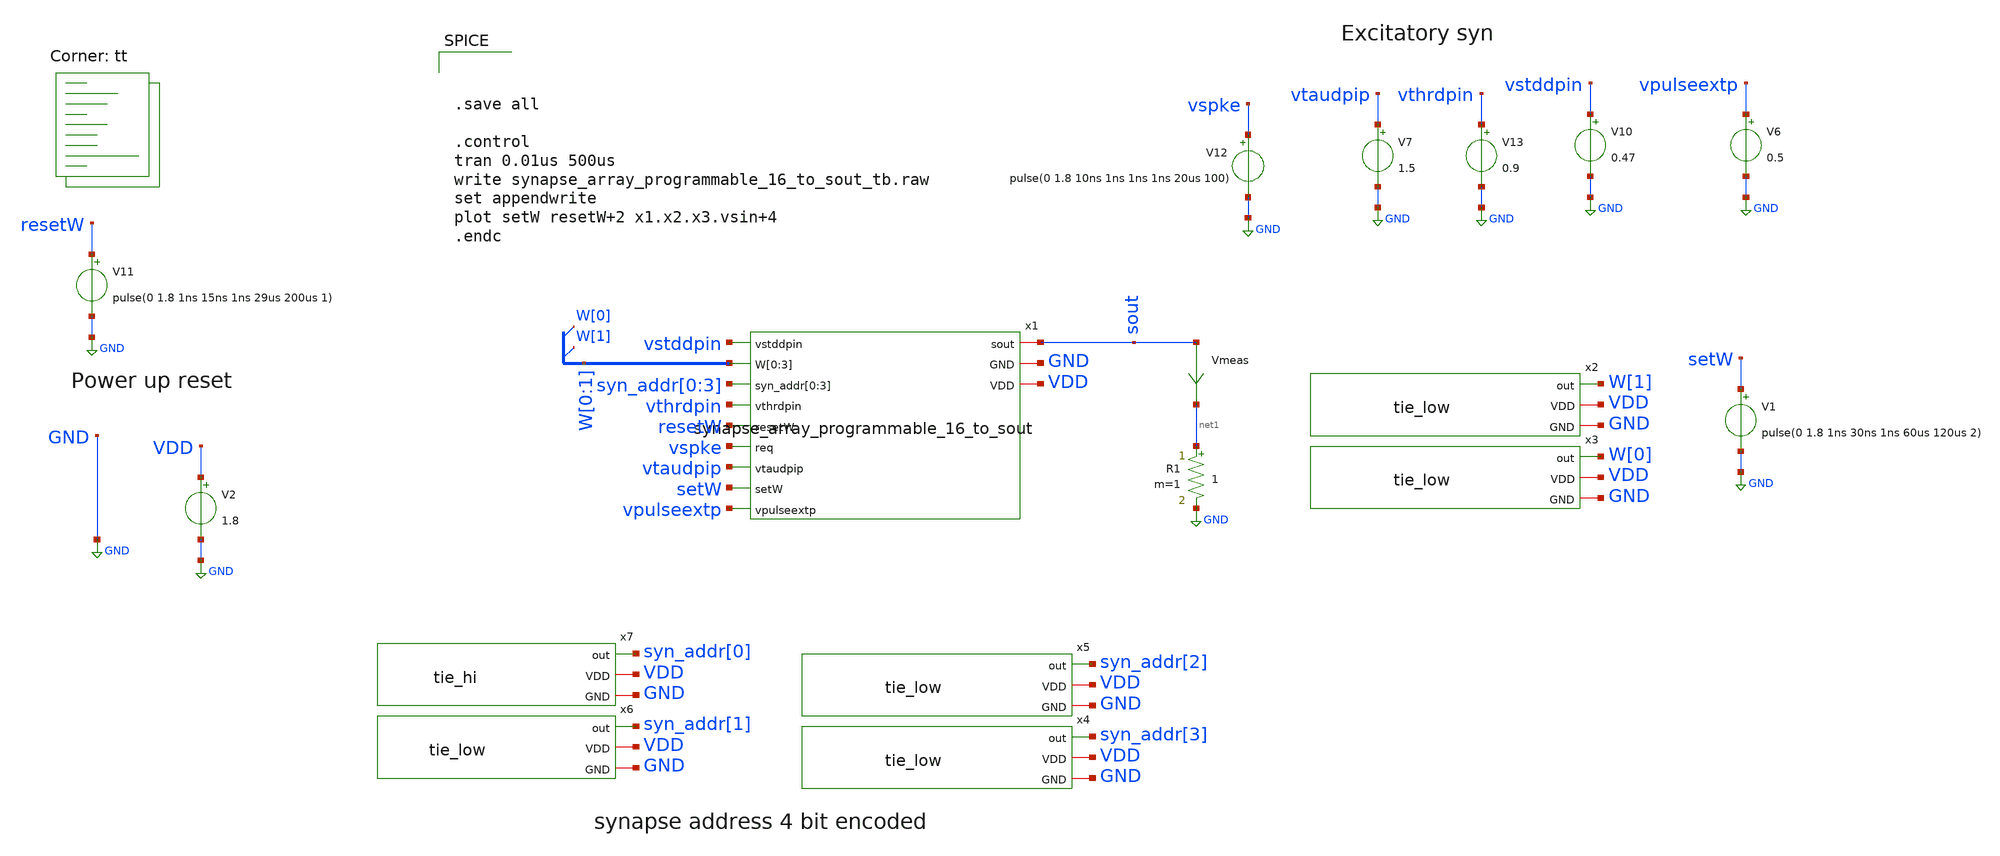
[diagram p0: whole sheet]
** sch_path: design/xschem/synapse_array_programmable_16_to_sout_tb.sch
**.subckt synapse_array_programmable_16_to_sout_tb
x1 vstddpin sout W[0] W[1] W[0] W[1] syn_addr[0] syn_addr[1] syn_addr[2] syn_addr[3] vthrdpin resetW
+ vspke vtaudpip setW vpulseextp GND VDD synapse_array_programmable_16_to_sout
R1 net1 GND 1 m=1
Vmeas sout net1 0
.save i(vmeas)
V11 resetW GND pulse(0 1.8 1ns 15ns 1ns 29us 200us 1)
V2 VDD GND 1.8
V7 vtaudpip GND 1.5
V13 vthrdpin GND 0.9
V10 vstddpin GND 0.47
V12 vspke GND pulse(0 1.8 10ns 1ns 1ns 1ns 20us 100)
V6 vpulseextp GND 0.5
V1 setW GND pulse(0 1.8 1ns 30ns 1ns 60us 120us 2)
x3 W[0] VDD GND tie_low
x2 W[1] VDD GND tie_low
x4 syn_addr[3] VDD GND tie_low
x5 syn_addr[2] VDD GND tie_low
x6 syn_addr[1] VDD GND tie_low
x7 syn_addr[0] VDD GND tie_hi
**** begin user architecture code



.save all

.control
tran 0.01us 500us
write synapse_array_programmable_16_to_sout_tb.raw
set appendwrite
plot setW resetW+2 x1.x2.x3.vsin+4
.endc




* Standard cell simulation files
.include $::SKYWATER_STDCELLS/sky130_fd_sc_hd.spice

* Power domains
VSTDCELL_PWR VPWR 0 DC 1.8
VSTDCELL_PB  VPB  0 DC 1.8
VSTDCELL_NB  VNB  0 DC 0
VSTDCELL_GND VGND 0 DC 0
.global VNB VGND VPB VPWR


.lib $::SKYWATER_MODELS/sky130.lib.spice tt
**** end user architecture code
**.ends

* expanding   symbol:  synapse_array_programmable_16_to_sout.sym # of pins=12
** sym_path: design/xschem/synapse_array_programmable_16_to_sout.sym
** sch_path: design/xschem/synapse_array_programmable_16_to_sout.sch
.subckt synapse_array_programmable_16_to_sout vstddpin sout W[0] W[1] W[2] W[3] syn_addr[0]
+ syn_addr[1] syn_addr[2] syn_addr[3] vthrdpin resetW req vtaudpip setW vpulseextp GND VDD
*.iopin GND
*.iopin VDD
*.ipin vpulseextp
*.ipin syn_addr[0],syn_addr[1],syn_addr[2],syn_addr[3]
*.ipin W[0],W[1],W[2],W[3]
*.ipin vthrdpin
*.ipin vtaudpip
*.ipin vstddpin
*.iopin sout
*.ipin setW
*.ipin resetW
*.ipin req
x1[0] sout vstddpin net1[15] resetW vthrdpin setW vtaudpip W[0] W[1] W[2] W[3] vpulseextp GND VDD
+ synapse_4bit_memory
x1[1] sout vstddpin net1[14] resetW vthrdpin setW vtaudpip W[0] W[1] W[2] W[3] vpulseextp GND VDD
+ synapse_4bit_memory
x1[2] sout vstddpin net1[13] resetW vthrdpin setW vtaudpip W[0] W[1] W[2] W[3] vpulseextp GND VDD
+ synapse_4bit_memory
x1[3] sout vstddpin net1[12] resetW vthrdpin setW vtaudpip W[0] W[1] W[2] W[3] vpulseextp GND VDD
+ synapse_4bit_memory
x1[4] sout vstddpin net1[11] resetW vthrdpin setW vtaudpip W[0] W[1] W[2] W[3] vpulseextp GND VDD
+ synapse_4bit_memory
x1[5] sout vstddpin net1[10] resetW vthrdpin setW vtaudpip W[0] W[1] W[2] W[3] vpulseextp GND VDD
+ synapse_4bit_memory
x1[6] sout vstddpin net1[9] resetW vthrdpin setW vtaudpip W[0] W[1] W[2] W[3] vpulseextp GND VDD
+ synapse_4bit_memory
x1[7] sout vstddpin net1[8] resetW vthrdpin setW vtaudpip W[0] W[1] W[2] W[3] vpulseextp GND VDD
+ synapse_4bit_memory
x1[8] sout vstddpin net1[7] resetW vthrdpin setW vtaudpip W[0] W[1] W[2] W[3] vpulseextp GND VDD
+ synapse_4bit_memory
x1[9] sout vstddpin net1[6] resetW vthrdpin setW vtaudpip W[0] W[1] W[2] W[3] vpulseextp GND VDD
+ synapse_4bit_memory
x1[10] sout vstddpin net1[5] resetW vthrdpin setW vtaudpip W[0] W[1] W[2] W[3] vpulseextp GND VDD
+ synapse_4bit_memory
x1[11] sout vstddpin net1[4] resetW vthrdpin setW vtaudpip W[0] W[1] W[2] W[3] vpulseextp GND VDD
+ synapse_4bit_memory
x1[12] sout vstddpin net1[3] resetW vthrdpin setW vtaudpip W[0] W[1] W[2] W[3] vpulseextp GND VDD
+ synapse_4bit_memory
x1[13] sout vstddpin net1[2] resetW vthrdpin setW vtaudpip W[0] W[1] W[2] W[3] vpulseextp GND VDD
+ synapse_4bit_memory
x1[14] sout vstddpin net1[1] resetW vthrdpin setW vtaudpip W[0] W[1] W[2] W[3] vpulseextp GND VDD
+ synapse_4bit_memory
x1[15] sout vstddpin net1[0] resetW vthrdpin setW vtaudpip W[0] W[1] W[2] W[3] vpulseextp GND VDD
+ synapse_4bit_memory
x3 syn_addr[0] syn_addr[1] syn_addr[2] syn_addr[3] D[15] D[14] D[13] D[12] D[11] D[10] D[9] D[8]
+ D[7] D[6] D[5] D[4] D[3] D[2] D[1] D[0] req req_syn VDD GND decoder_4_to_16
x4[0] D[0] req_syn GND GND VDD VDD net1[15] sky130_fd_sc_hd__and2_1
x4[1] D[1] req_syn GND GND VDD VDD net1[14] sky130_fd_sc_hd__and2_1
x4[2] D[2] req_syn GND GND VDD VDD net1[13] sky130_fd_sc_hd__and2_1
x4[3] D[3] req_syn GND GND VDD VDD net1[12] sky130_fd_sc_hd__and2_1
x4[4] D[4] req_syn GND GND VDD VDD net1[11] sky130_fd_sc_hd__and2_1
x4[5] D[5] req_syn GND GND VDD VDD net1[10] sky130_fd_sc_hd__and2_1
x4[6] D[6] req_syn GND GND VDD VDD net1[9] sky130_fd_sc_hd__and2_1
x4[7] D[7] req_syn GND GND VDD VDD net1[8] sky130_fd_sc_hd__and2_1
x4[8] D[8] req_syn GND GND VDD VDD net1[7] sky130_fd_sc_hd__and2_1
x4[9] D[9] req_syn GND GND VDD VDD net1[6] sky130_fd_sc_hd__and2_1
x4[10] D[10] req_syn GND GND VDD VDD net1[5] sky130_fd_sc_hd__and2_1
x4[11] D[11] req_syn GND GND VDD VDD net1[4] sky130_fd_sc_hd__and2_1
x4[12] D[12] req_syn GND GND VDD VDD net1[3] sky130_fd_sc_hd__and2_1
x4[13] D[13] req_syn GND GND VDD VDD net1[2] sky130_fd_sc_hd__and2_1
x4[14] D[14] req_syn GND GND VDD VDD net1[1] sky130_fd_sc_hd__and2_1
x4[15] D[15] req_syn GND GND VDD VDD net1[0] sky130_fd_sc_hd__and2_1
.ends


* expanding   symbol:  tie_low.sym # of pins=3
** sym_path: design/xschem/tie_low.sym
** sch_path: design/xschem/tie_low.sch
.subckt tie_low out VDD GND
*.iopin VDD
*.iopin GND
*.opin out
XM4 net1 net1 VDD VDD sky130_fd_pr__pfet_01v8 L=0.15 W=1 nf=1 ad='int((nf+1)/2) * W/nf * 0.29' as='int((nf+2)/2) * W/nf * 0.29'
+ pd='2*int((nf+1)/2) * (W/nf + 0.29)' ps='2*int((nf+2)/2) * (W/nf + 0.29)' nrd='0.29 / W' nrs='0.29 / W'
+ sa=0 sb=0 sd=0 mult=1 m=1
XM2 out net1 GND GND sky130_fd_pr__nfet_01v8 L=0.15 W=0.65 nf=1 ad='int((nf+1)/2) * W/nf * 0.29' as='int((nf+2)/2) * W/nf * 0.29'
+ pd='2*int((nf+1)/2) * (W/nf + 0.29)' ps='2*int((nf+2)/2) * (W/nf + 0.29)' nrd='0.29 / W' nrs='0.29 / W'
+ sa=0 sb=0 sd=0 mult=1 m=1
.ends


* expanding   symbol:  tie_hi.sym # of pins=3
** sym_path: design/xschem/tie_hi.sym
** sch_path: design/xschem/tie_hi.sch
.subckt tie_hi out VDD GND
*.iopin VDD
*.iopin GND
*.opin out
XM4 out net1 VDD VDD sky130_fd_pr__pfet_01v8 L=0.15 W=1 nf=1 ad='int((nf+1)/2) * W/nf * 0.29' as='int((nf+2)/2) * W/nf * 0.29'
+ pd='2*int((nf+1)/2) * (W/nf + 0.29)' ps='2*int((nf+2)/2) * (W/nf + 0.29)' nrd='0.29 / W' nrs='0.29 / W'
+ sa=0 sb=0 sd=0 mult=1 m=1
XM2 net1 net1 GND GND sky130_fd_pr__nfet_01v8 L=0.15 W=0.65 nf=1 ad='int((nf+1)/2) * W/nf * 0.29' as='int((nf+2)/2) * W/nf * 0.29'
+ pd='2*int((nf+1)/2) * (W/nf + 0.29)' ps='2*int((nf+2)/2) * (W/nf + 0.29)' nrd='0.29 / W' nrs='0.29 / W'
+ sa=0 sb=0 sd=0 mult=1 m=1
.ends


* expanding   symbol:  synapse_4bit_memory.sym # of pins=11
** sym_path: design/xschem/synapse_4bit_memory.sym
** sch_path: design/xschem/synapse_4bit_memory.sch
.subckt synapse_4bit_memory sout vstddpin spk resetW vthrdpin setW vtaudpip W[0] W[1] W[2] W[3]
+ vpulseextp GND VDD
*.iopin GND
*.iopin VDD
*.ipin vpulseextp
*.ipin spk
*.ipin vthrdpin
*.ipin vtaudpip
*.ipin vstddpin
*.ipin W[0],W[1],W[2],W[3]
*.ipin setW
*.ipin resetW
*.iopin sout
x1 vpulseextp spk GND spke VDD spike_extender
x3 vtaudpip sout vthrdpin spke vstddpin GND VDD net1[3] net1[2] net1[1] net1[0] dpi_syn_exc_4bit_fc
x2[0] setW W[0] net2 GND GND VDD VDD net1[3] sky130_fd_sc_hd__dfrtp_1
x2[1] setW W[1] net2 GND GND VDD VDD net1[2] sky130_fd_sc_hd__dfrtp_1
x2[2] setW W[2] net2 GND GND VDD VDD net1[1] sky130_fd_sc_hd__dfrtp_1
x2[3] setW W[3] net2 GND GND VDD VDD net1[0] sky130_fd_sc_hd__dfrtp_1
x11 resetW GND GND VDD VDD net2 sky130_fd_sc_hd__inv_1
.ends


* expanding   symbol:  decoder_4_to_16.sym # of pins=6
** sym_path: design/xschem/decoder_4_to_16.sym
** sch_path: design/xschem/decoder_4_to_16.sch
.subckt decoder_4_to_16 A[0] A[1] A[2] A[3] D[0] D[1] D[2] D[3] D[4] D[5] D[6] D[7] D[8] D[9] D[10]
+ D[11] D[12] D[13] D[14] D[15] req req_syn dVDD dGND
*.ipin A[0],A[1],A[2],A[3]
*.ipin req
*.opin D[0],D[1],D[2],D[3],D[4],D[5],D[6],D[7],D[8],D[9],D[10],D[11],D[12],D[13],D[14],D[15]
*.opin req_syn
*.iopin dVDD
*.iopin dGND
x21 req dGND dGND dVDD dVDD net5 sky130_fd_sc_hd__inv_1
x22 net5 dGND dGND dVDD dVDD net6 sky130_fd_sc_hd__inv_1
x23 net6 dGND dGND dVDD dVDD net7 sky130_fd_sc_hd__inv_1
x24 net7 dGND dGND dVDD dVDD req_syn sky130_fd_sc_hd__inv_1
x20 A[3] A[2] A[1] A[0] dGND dGND dVDD dVDD D[15] sky130_fd_sc_hd__and4_1
x19 A[3] A[2] A[1] net4 dGND dGND dVDD dVDD D[14] sky130_fd_sc_hd__and4_1
x18 A[3] A[2] net3 A[0] dGND dGND dVDD dVDD D[13] sky130_fd_sc_hd__and4_1
x17 A[3] A[2] net3 net4 dGND dGND dVDD dVDD D[12] sky130_fd_sc_hd__and4_1
x16 A[3] net2 A[1] A[0] dGND dGND dVDD dVDD D[11] sky130_fd_sc_hd__and4_1
x15 A[3] net2 A[1] net4 dGND dGND dVDD dVDD D[10] sky130_fd_sc_hd__and4_1
x13 A[3] net2 net3 A[0] dGND dGND dVDD dVDD D[9] sky130_fd_sc_hd__and4_1
x4 A[3] net2 net3 net4 dGND dGND dVDD dVDD D[8] sky130_fd_sc_hd__and4_1
x5 net1 A[2] A[1] A[0] dGND dGND dVDD dVDD D[7] sky130_fd_sc_hd__and4_1
x6 net1 A[2] A[1] net4 dGND dGND dVDD dVDD D[6] sky130_fd_sc_hd__and4_1
x8 net1 A[2] net3 net4 dGND dGND dVDD dVDD D[4] sky130_fd_sc_hd__and4_1
x9 net1 net2 A[1] net4 dGND dGND dVDD dVDD D[2] sky130_fd_sc_hd__and4_1
x10 net1 net2 net3 net4 dGND dGND dVDD dVDD D[0] sky130_fd_sc_hd__and4_1
x11 net1 net2 net3 A[0] dGND dGND dVDD dVDD D[1] sky130_fd_sc_hd__and4_1
x12 net1 net2 A[1] A[0] dGND dGND dVDD dVDD D[3] sky130_fd_sc_hd__and4_1
x14 net1 A[2] net3 A[0] dGND dGND dVDD dVDD D[5] sky130_fd_sc_hd__and4_1
x1 A[3] dGND dGND dVDD dVDD net1 sky130_fd_sc_hd__inv_4
x2 A[2] dGND dGND dVDD dVDD net2 sky130_fd_sc_hd__inv_4
x3 A[1] dGND dGND dVDD dVDD net3 sky130_fd_sc_hd__inv_4
x7 A[0] dGND dGND dVDD dVDD net4 sky130_fd_sc_hd__inv_4
.ends


* expanding   symbol:  spike_extender.sym # of pins=5
** sym_path: design/xschem/spike_extender.sym
** sch_path: design/xschem/spike_extender.sch
.subckt spike_extender vpulseextp spk GND spkext VDD
*.iopin GND
*.iopin VDD
*.ipin spk
*.opin spkext
*.ipin vpulseextp
XM1 net1 spk GND GND sky130_fd_pr__nfet_01v8 L=0.15 W=0.65 nf=1 ad='int((nf+1)/2) * W/nf * 0.29' as='int((nf+2)/2) * W/nf * 0.29'
+ pd='2*int((nf+1)/2) * (W/nf + 0.29)' ps='2*int((nf+2)/2) * (W/nf + 0.29)' nrd='0.29 / W' nrs='0.29 / W'
+ sa=0 sb=0 sd=0 mult=1 m=1
XM6 net1 vpulseextp VDD VDD sky130_fd_pr__pfet_01v8 L=2 W=1 nf=1 ad='int((nf+1)/2) * W/nf * 0.29' as='int((nf+2)/2) * W/nf * 0.29'
+ pd='2*int((nf+1)/2) * (W/nf + 0.29)' ps='2*int((nf+2)/2) * (W/nf + 0.29)' nrd='0.29 / W' nrs='0.29 / W'
+ sa=0 sb=0 sd=0 mult=1 m=1
XM5 net3 net2 GND GND sky130_fd_pr__nfet_01v8 L=0.15 W=0.65 nf=1 ad='int((nf+1)/2) * W/nf * 0.29' as='int((nf+2)/2) * W/nf * 0.29'
+ pd='2*int((nf+1)/2) * (W/nf + 0.29)' ps='2*int((nf+2)/2) * (W/nf + 0.29)' nrd='0.29 / W' nrs='0.29 / W'
+ sa=0 sb=0 sd=0 mult=1 m=1
XM8 spkext net3 GND GND sky130_fd_pr__nfet_01v8 L=0.15 W=0.65 nf=1 ad='int((nf+1)/2) * W/nf * 0.29' as='int((nf+2)/2) * W/nf * 0.29'
+ pd='2*int((nf+1)/2) * (W/nf + 0.29)' ps='2*int((nf+2)/2) * (W/nf + 0.29)' nrd='0.29 / W' nrs='0.29 / W'
+ sa=0 sb=0 sd=0 mult=1 m=1
XM4 net3 net2 VDD VDD sky130_fd_pr__pfet_01v8 L=0.15 W=1.0 nf=1 ad='int((nf+1)/2) * W/nf * 0.29' as='int((nf+2)/2) * W/nf * 0.29'
+ pd='2*int((nf+1)/2) * (W/nf + 0.29)' ps='2*int((nf+2)/2) * (W/nf + 0.29)' nrd='0.29 / W' nrs='0.29 / W'
+ sa=0 sb=0 sd=0 mult=1 m=1
XM7 spkext net3 VDD VDD sky130_fd_pr__pfet_01v8 L=0.15 W=1.0 nf=1 ad='int((nf+1)/2) * W/nf * 0.29' as='int((nf+2)/2) * W/nf * 0.29'
+ pd='2*int((nf+1)/2) * (W/nf + 0.29)' ps='2*int((nf+2)/2) * (W/nf + 0.29)' nrd='0.29 / W' nrs='0.29 / W'
+ sa=0 sb=0 sd=0 mult=1 m=1
XM2 net2 net1 GND GND sky130_fd_pr__nfet_01v8 L=0.15 W=0.65 nf=1 ad='int((nf+1)/2) * W/nf * 0.29' as='int((nf+2)/2) * W/nf * 0.29'
+ pd='2*int((nf+1)/2) * (W/nf + 0.29)' ps='2*int((nf+2)/2) * (W/nf + 0.29)' nrd='0.29 / W' nrs='0.29 / W'
+ sa=0 sb=0 sd=0 mult=1 m=1
XM3 net2 net1 VDD VDD sky130_fd_pr__pfet_01v8 L=0.15 W=1.0 nf=1 ad='int((nf+1)/2) * W/nf * 0.29' as='int((nf+2)/2) * W/nf * 0.29'
+ pd='2*int((nf+1)/2) * (W/nf + 0.29)' ps='2*int((nf+2)/2) * (W/nf + 0.29)' nrd='0.29 / W' nrs='0.29 / W'
+ sa=0 sb=0 sd=0 mult=1 m=1
XM9 GND net1 GND GND sky130_fd_pr__nfet_01v8 L=1 W=0.65 nf=1 ad='int((nf+1)/2) * W/nf * 0.29' as='int((nf+2)/2) * W/nf * 0.29'
+ pd='2*int((nf+1)/2) * (W/nf + 0.29)' ps='2*int((nf+2)/2) * (W/nf + 0.29)' nrd='0.29 / W' nrs='0.29 / W'
+ sa=0 sb=0 sd=0 mult=1 m=1
.ends


* expanding   symbol:  dpi_syn_exc_4bit_fc.sym # of pins=8
** sym_path: design/xschem/dpi_syn_exc_4bit_fc.sym
** sch_path: design/xschem/dpi_syn_exc_4bit_fc.sch
.subckt dpi_syn_exc_4bit_fc vtau sout vthn spk vstdn GND VDD weight[0] weight[1] weight[2] weight[3]
*.iopin GND
*.iopin VDD
*.iopin vtau
*.iopin vstdn
*.ipin spk
*.opin sout
*.iopin vthn
*.ipin weight[0],weight[1],weight[2],weight[3]
XM2 net3 spk net1 GND sky130_fd_pr__nfet_01v8 L=0.25 W=0.8 nf=1 ad='int((nf+1)/2) * W/nf * 0.29' as='int((nf+2)/2) * W/nf * 0.29'
+ pd='2*int((nf+1)/2) * (W/nf + 0.29)' ps='2*int((nf+2)/2) * (W/nf + 0.29)' nrd='0.29 / W' nrs='0.29 / W'
+ sa=0 sb=0 sd=0 mult=1 m=1
XC1 vsin VDD sky130_fd_pr__cap_mim_m3_1 W=5 L=5 MF=1 m=1
XM5 vsin vtau VDD VDD sky130_fd_pr__pfet_01v8 L=0.2 W=1.2 nf=1 ad='int((nf+1)/2) * W/nf * 0.29' as='int((nf+2)/2) * W/nf * 0.29'
+ pd='2*int((nf+1)/2) * (W/nf + 0.29)' ps='2*int((nf+2)/2) * (W/nf + 0.29)' nrd='0.29 / W' nrs='0.29 / W'
+ sa=0 sb=0 sd=0 mult=1 m=1
XM6 sout vsin VDD VDD sky130_fd_pr__pfet_01v8 L=0.2 W=1.2 nf=1 ad='int((nf+1)/2) * W/nf * 0.29' as='int((nf+2)/2) * W/nf * 0.29'
+ pd='2*int((nf+1)/2) * (W/nf + 0.29)' ps='2*int((nf+2)/2) * (W/nf + 0.29)' nrd='0.29 / W' nrs='0.29 / W'
+ sa=0 sb=0 sd=0 mult=1 m=1
XM1 net1 vstdn net2 GND sky130_fd_pr__nfet_01v8 L=0.5 W=0.8 nf=1 ad='int((nf+1)/2) * W/nf * 0.29' as='int((nf+2)/2) * W/nf * 0.29'
+ pd='2*int((nf+1)/2) * (W/nf + 0.29)' ps='2*int((nf+2)/2) * (W/nf + 0.29)' nrd='0.29 / W' nrs='0.29 / W'
+ sa=0 sb=0 sd=0 mult=1 m=1
XM4 vsin vsin net3 GND sky130_fd_pr__nfet_01v8 L=0.25 W=0.8 nf=1 ad='int((nf+1)/2) * W/nf * 0.29' as='int((nf+2)/2) * W/nf * 0.29'
+ pd='2*int((nf+1)/2) * (W/nf + 0.29)' ps='2*int((nf+2)/2) * (W/nf + 0.29)' nrd='0.29 / W' nrs='0.29 / W'
+ sa=0 sb=0 sd=0 mult=1 m=1
XM3 VDD vthn net3 GND sky130_fd_pr__nfet_01v8 L=0.25 W=0.8 nf=1 ad='int((nf+1)/2) * W/nf * 0.29' as='int((nf+2)/2) * W/nf * 0.29'
+ pd='2*int((nf+1)/2) * (W/nf + 0.29)' ps='2*int((nf+2)/2) * (W/nf + 0.29)' nrd='0.29 / W' nrs='0.29 / W'
+ sa=0 sb=0 sd=0 mult=1 m=1
XM7 net1 vstdn net4 GND sky130_fd_pr__nfet_01v8 L=2.0 W=0.8 nf=1 ad='int((nf+1)/2) * W/nf * 0.29' as='int((nf+2)/2) * W/nf * 0.29'
+ pd='2*int((nf+1)/2) * (W/nf + 0.29)' ps='2*int((nf+2)/2) * (W/nf + 0.29)' nrd='0.29 / W' nrs='0.29 / W'
+ sa=0 sb=0 sd=0 mult=1 m=1
XM8 net1 vstdn net5 GND sky130_fd_pr__nfet_01v8 L=4.0 W=0.8 nf=1 ad='int((nf+1)/2) * W/nf * 0.29' as='int((nf+2)/2) * W/nf * 0.29'
+ pd='2*int((nf+1)/2) * (W/nf + 0.29)' ps='2*int((nf+2)/2) * (W/nf + 0.29)' nrd='0.29 / W' nrs='0.29 / W'
+ sa=0 sb=0 sd=0 mult=1 m=1
XM9 net1 vstdn net6 GND sky130_fd_pr__nfet_01v8 L=8.0 W=0.8 nf=1 ad='int((nf+1)/2) * W/nf * 0.29' as='int((nf+2)/2) * W/nf * 0.29'
+ pd='2*int((nf+1)/2) * (W/nf + 0.29)' ps='2*int((nf+2)/2) * (W/nf + 0.29)' nrd='0.29 / W' nrs='0.29 / W'
+ sa=0 sb=0 sd=0 mult=1 m=1
XM10 net2 weight[0] GND GND sky130_fd_pr__nfet_01v8 L=0.25 W=0.8 nf=1 ad='int((nf+1)/2) * W/nf * 0.29'
+ as='int((nf+2)/2) * W/nf * 0.29' pd='2*int((nf+1)/2) * (W/nf + 0.29)' ps='2*int((nf+2)/2) * (W/nf + 0.29)'
+ nrd='0.29 / W' nrs='0.29 / W' sa=0 sb=0 sd=0 mult=1 m=1
XM11 net4 weight[1] GND GND sky130_fd_pr__nfet_01v8 L=0.25 W=0.8 nf=1 ad='int((nf+1)/2) * W/nf * 0.29'
+ as='int((nf+2)/2) * W/nf * 0.29' pd='2*int((nf+1)/2) * (W/nf + 0.29)' ps='2*int((nf+2)/2) * (W/nf + 0.29)'
+ nrd='0.29 / W' nrs='0.29 / W' sa=0 sb=0 sd=0 mult=1 m=1
XM12 net5 weight[2] GND GND sky130_fd_pr__nfet_01v8 L=0.25 W=0.8 nf=1 ad='int((nf+1)/2) * W/nf * 0.29'
+ as='int((nf+2)/2) * W/nf * 0.29' pd='2*int((nf+1)/2) * (W/nf + 0.29)' ps='2*int((nf+2)/2) * (W/nf + 0.29)'
+ nrd='0.29 / W' nrs='0.29 / W' sa=0 sb=0 sd=0 mult=1 m=1
XM13 net6 weight[3] GND GND sky130_fd_pr__nfet_01v8 L=0.25 W=0.8 nf=1 ad='int((nf+1)/2) * W/nf * 0.29'
+ as='int((nf+2)/2) * W/nf * 0.29' pd='2*int((nf+1)/2) * (W/nf + 0.29)' ps='2*int((nf+2)/2) * (W/nf + 0.29)'
+ nrd='0.29 / W' nrs='0.29 / W' sa=0 sb=0 sd=0 mult=1 m=1
.ends

.GLOBAL GND
.end
